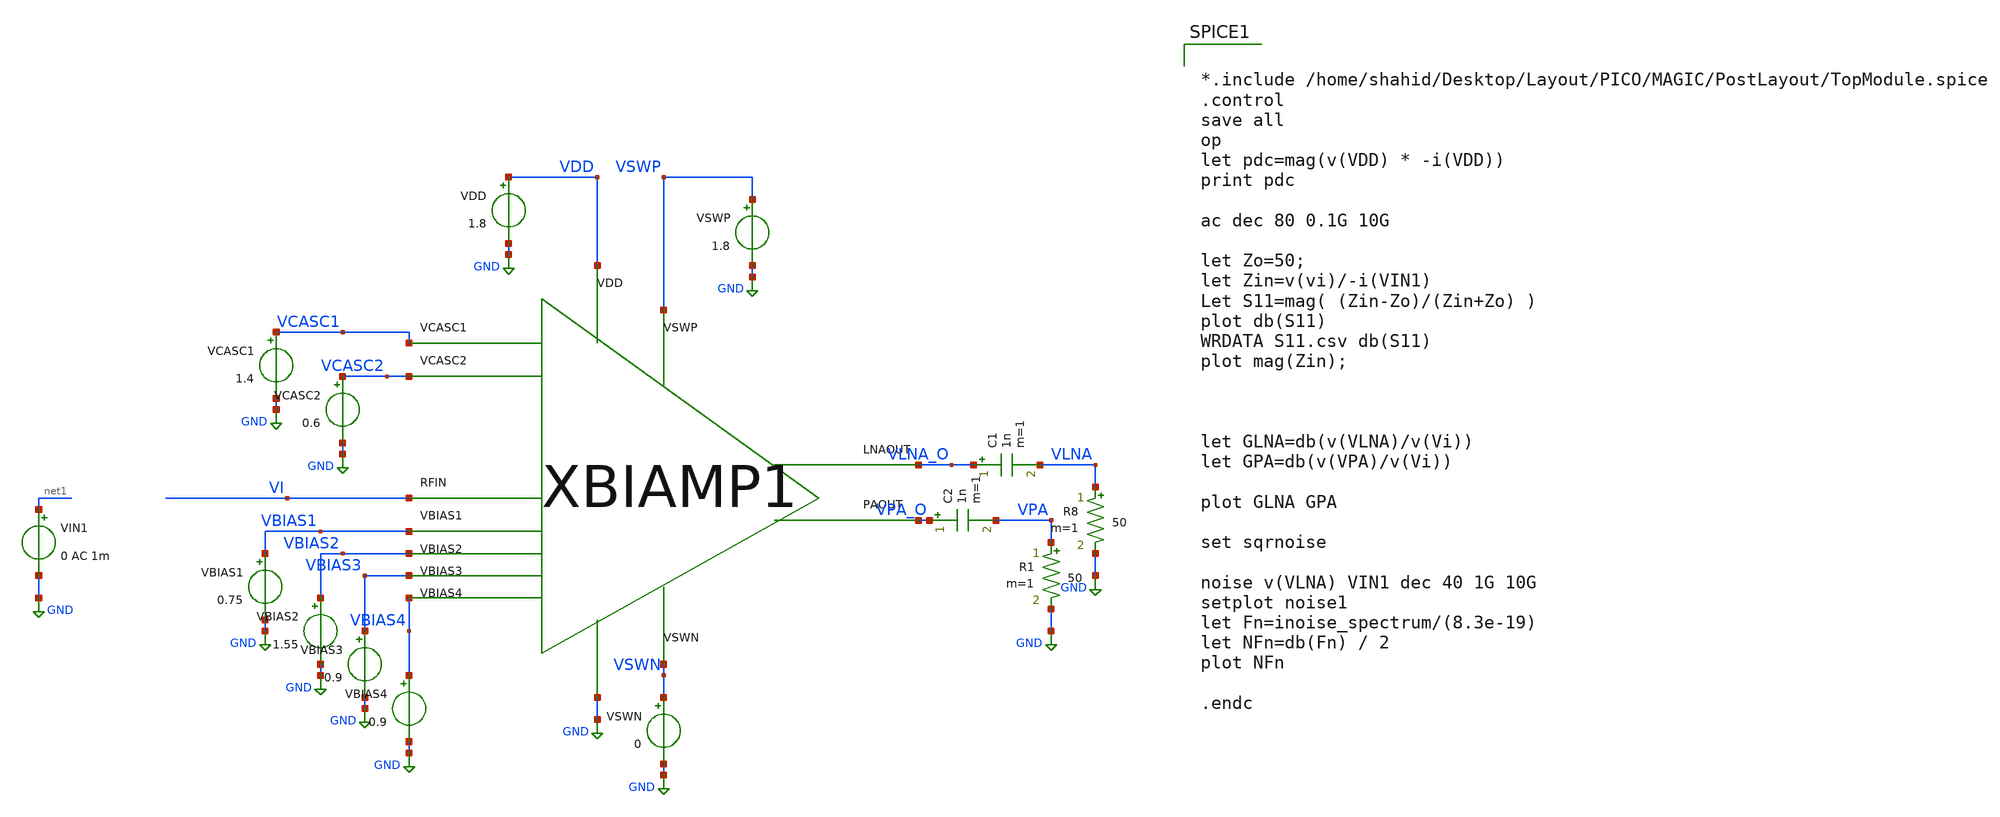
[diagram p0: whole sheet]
** sch_path: xschem/Top_PostLayout.sch
**.subckt Top_PostLayout
XBIAMP1 VCASC1 VCASC2 VI VBIAS1 VBIAS2 VBIAS3 VBIAS4 VDD VSWP GND VSWN VPA_O VLNA_O Top_PostLayout
VCASC1 VCASC1 GND 1.4
VCASC2 VCASC2 GND 0.6
VDD VDD GND 1.8
VSWP VSWP GND 1.8
VIN1 net1 GND 0 AC 1m
VBIAS1 VBIAS1 GND 0.75
VBIAS2 VBIAS2 GND 1.55
VBIAS3 VBIAS3 GND 0.9
VBIAS4 VBIAS4 GND 0.9
VSWN VSWN GND 0
C1 VLNA_O VLNA 1n m=1
R8 VLNA GND 50 m=1
C2 VPA_O VPA 1n m=1
R1 VPA GND 50 m=1
**** begin user architecture code

.lib $::SKYWATER_MODELS/sky130.lib.spice tt



*.include /home/shahid/Desktop/Layout/PICO/MAGIC/PostLayout/TopModule.spice
.control
save all
op
let pdc=mag(v(VDD) * -i(VDD))
print pdc

ac dec 80 0.1G 10G

let Zo=50;
let Zin=v(vi)/-i(VIN1)
Let S11=mag( (Zin-Zo)/(Zin+Zo) )
plot db(S11)
WRDATA S11.csv db(S11)
plot mag(Zin);



let GLNA=db(v(VLNA)/v(Vi))
let GPA=db(v(VPA)/v(Vi))

plot GLNA GPA

set sqrnoise

noise v(VLNA) VIN1 dec 40 1G 10G
setplot noise1
let Fn=inoise_spectrum/(8.3e-19)
let NFn=db(Fn) / 2
plot NFn

.endc


**** end user architecture code
**.ends
.GLOBAL GND
.end
